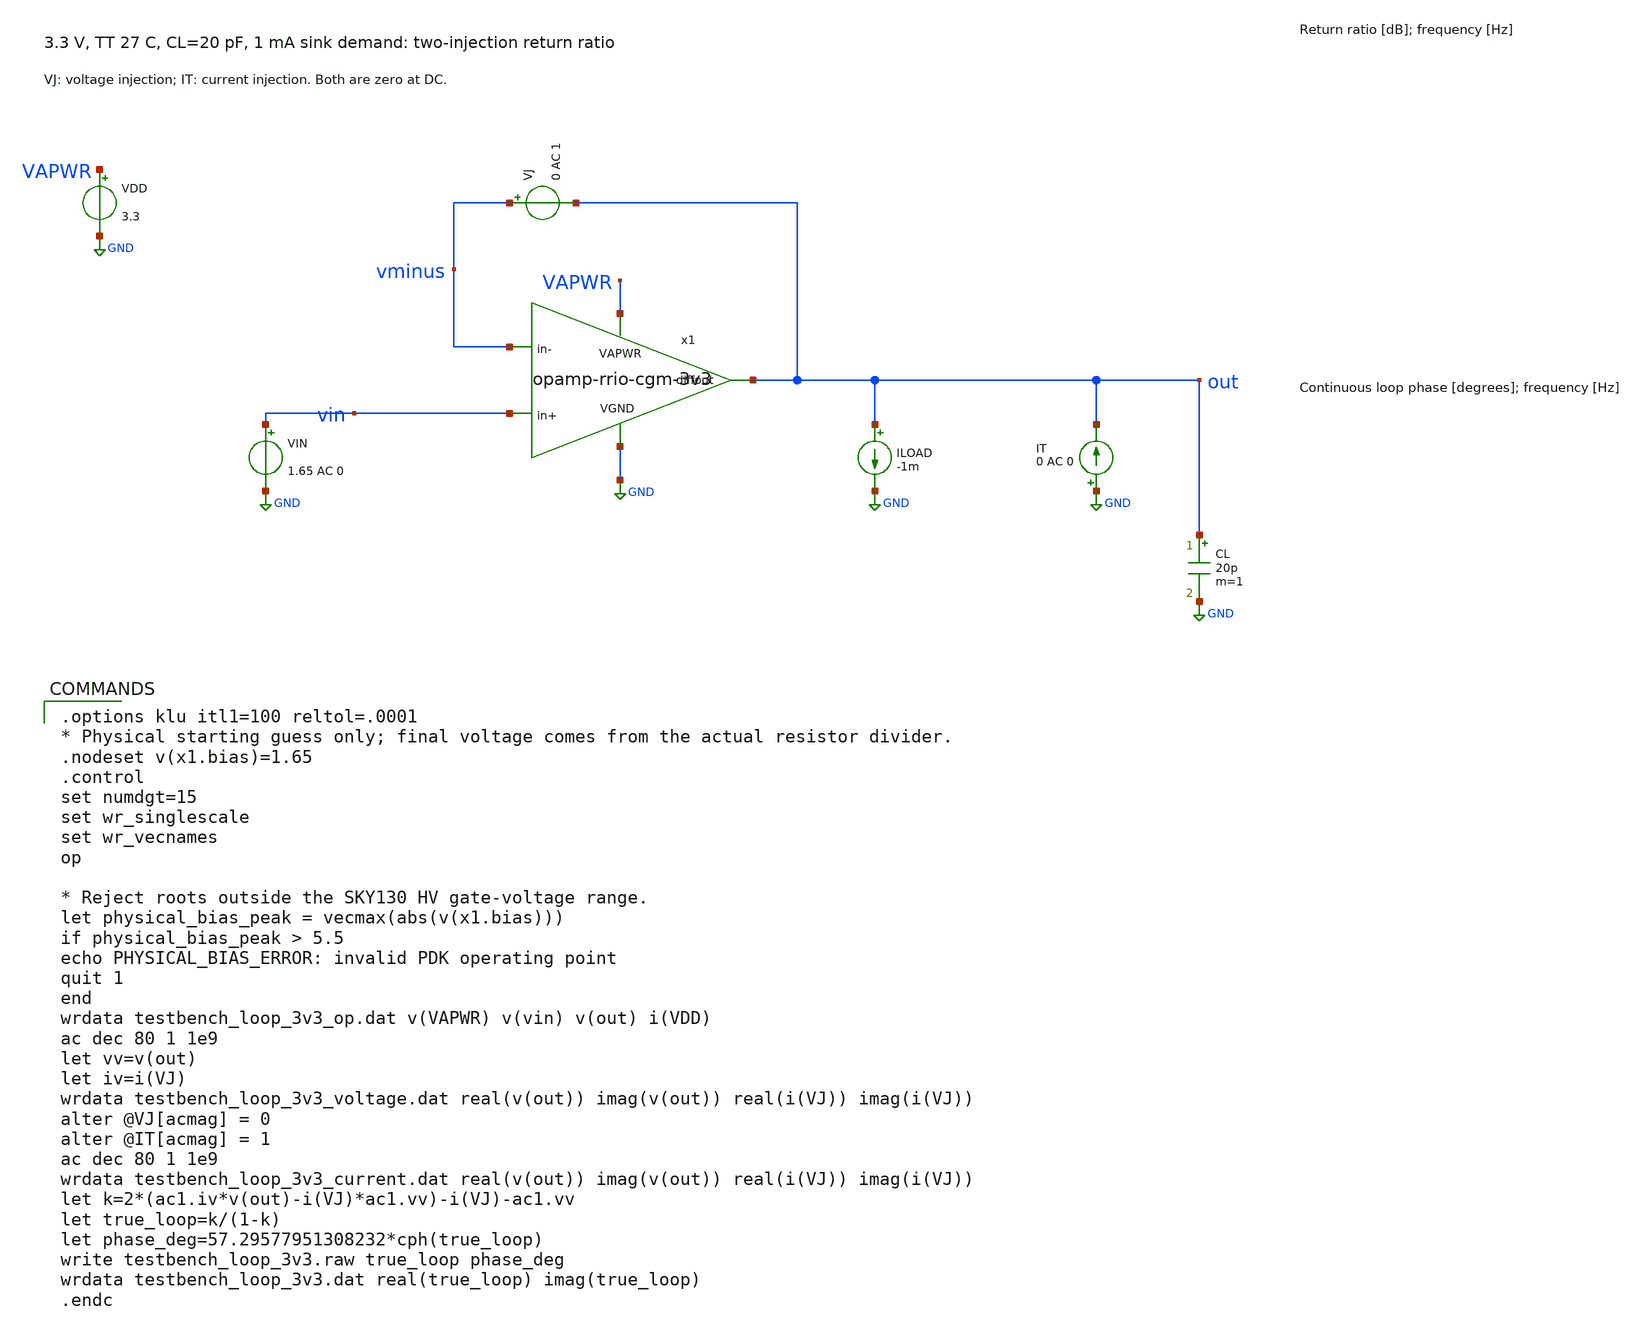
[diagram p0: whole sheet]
** sch_path: xschem/testbench_loop_3v3.sch
**.subckt testbench_loop_3v3
x1 VAPWR out vin vminus GND opamp-rrio-cgm-3v3
VDD VAPWR GND 3.3
VIN vin GND 1.65 AC 0
VJ vminus out 0 AC 1
ILOAD out GND -1m
IT GND out 0 AC 0
CL out GND 20p m=1
**** begin user architecture code
 .lib $::SKYWATER_MODELS/sky130.lib.spice tt

.options klu itl1=100 reltol=.0001
* Physical starting guess only; final voltage comes from the actual resistor divider.
.nodeset v(x1.bias)=1.65
.control
set numdgt=15
set wr_singlescale
set wr_vecnames
op

* Reject roots outside the SKY130 HV gate-voltage range.
let physical_bias_peak = vecmax(abs(v(x1.bias)))
if physical_bias_peak > 5.5
echo PHYSICAL_BIAS_ERROR: invalid PDK operating point
quit 1
end
wrdata testbench_loop_3v3_op.dat v(VAPWR) v(vin) v(out) i(VDD)
ac dec 80 1 1e9
let vv=v(out)
let iv=i(VJ)
wrdata testbench_loop_3v3_voltage.dat real(v(out)) imag(v(out)) real(i(VJ)) imag(i(VJ))
alter @VJ[acmag] = 0
alter @IT[acmag] = 1
ac dec 80 1 1e9
wrdata testbench_loop_3v3_current.dat real(v(out)) imag(v(out)) real(i(VJ)) imag(i(VJ))
let k=2*(ac1.iv*v(out)-i(VJ)*ac1.vv)-i(VJ)-ac1.vv
let true_loop=k/(1-k)
let phase_deg=57.29577951308232*cph(true_loop)
write testbench_loop_3v3.raw true_loop phase_deg
wrdata testbench_loop_3v3.dat real(true_loop) imag(true_loop)
.endc

**** end user architecture code
**.ends
.GLOBAL GND
.end
